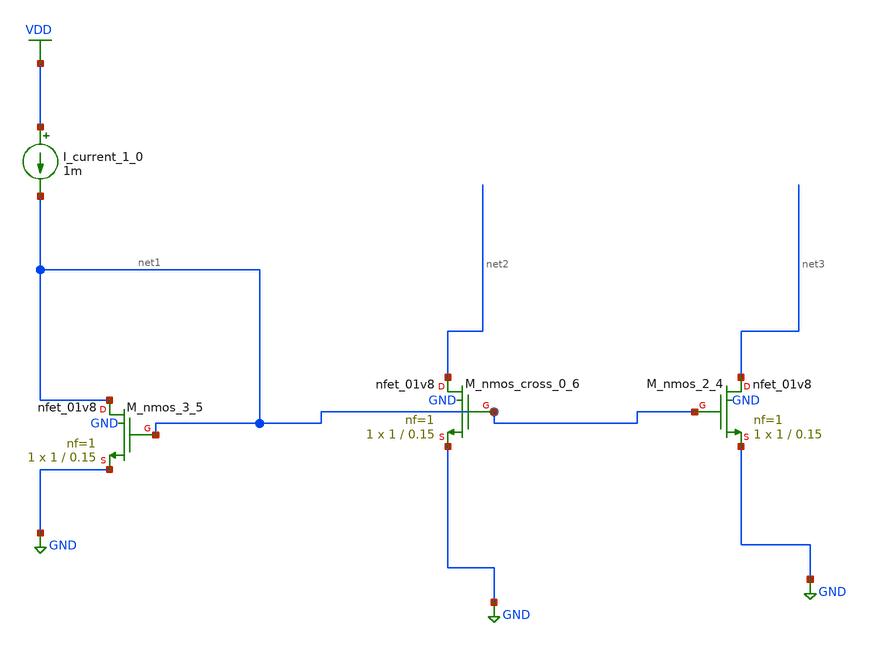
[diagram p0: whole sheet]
** sch_path: schematics/AMSNet/760.sch
**.subckt 760
I_current_1_0 VDD net1 1m
XM_nmos_2_4 net3 net1 GND GND sky130_fd_pr__nfet_01v8 L=0.15 W=1 nf=1 ad='int((1 + 1)/2) * 1 / 1 * 0.29'
+ as='int((1 + 2)/2) * 1 / 1 * 0.29' pd='2*int((1 + 1)/2) * (1 / 1 + 0.29)' ps='2*int((1 + 2)/2) * (1 / 1 + 0.29)'
+ nrd='0.29 / 1 ' nrs='0.29 / 1 ' sa=0 sb=0 sd=0 mult=1 m=1
XM_nmos_3_5 net1 net1 GND GND sky130_fd_pr__nfet_01v8 L=0.15 W=1 nf=1 ad='int((1 + 1)/2) * 1 / 1 * 0.29'
+ as='int((1 + 2)/2) * 1 / 1 * 0.29' pd='2*int((1 + 1)/2) * (1 / 1 + 0.29)' ps='2*int((1 + 2)/2) * (1 / 1 + 0.29)'
+ nrd='0.29 / 1 ' nrs='0.29 / 1 ' sa=0 sb=0 sd=0 mult=1 m=1
XM_nmos_cross_0_6 net2 net1 GND GND sky130_fd_pr__nfet_01v8 L=0.15 W=1 nf=1 ad='int((1 + 1)/2) * 1 / 1 * 0.29'
+ as='int((1 + 2)/2) * 1 / 1 * 0.29' pd='2*int((1 + 1)/2) * (1 / 1 + 0.29)' ps='2*int((1 + 2)/2) * (1 / 1 + 0.29)'
+ nrd='0.29 / 1 ' nrs='0.29 / 1 ' sa=0 sb=0 sd=0 mult=1 m=1
**.ends
.GLOBAL GND
.GLOBAL VDD
.end
